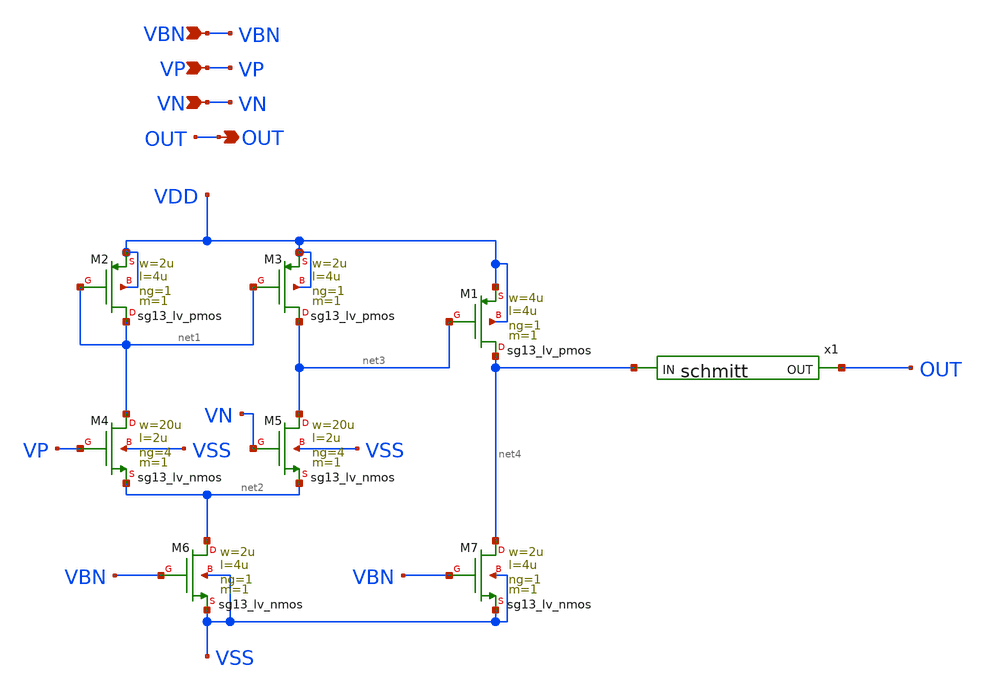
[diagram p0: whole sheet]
** sch_path: design/blocks/comparator/schematic/comp_sup.sch
**.subckt comp_sup OUT VN VP VBN
*.opin OUT
*.ipin VN
*.ipin VP
*.ipin VBN
XM2 net1 net1 VDD VDD sg13_lv_pmos w=2u l=4u ng=1 m=1 mm_ok=1
XM3 net3 net1 VDD VDD sg13_lv_pmos w=2u l=4u ng=1 m=1 mm_ok=1
XM4 net1 VP net2 VSS sg13_lv_nmos w=20u l=2u ng=4 m=1 mm_ok=1
XM5 net3 VN net2 VSS sg13_lv_nmos w=20u l=2u ng=4 m=1 mm_ok=1
XM6 net2 VBN VSS VSS sg13_lv_nmos w=2u l=4u ng=1 m=1 mm_ok=1
XM1 net4 net3 VDD VDD sg13_lv_pmos w=4u l=4u ng=1 m=1 mm_ok=1
XM7 net4 VBN VSS VSS sg13_lv_nmos w=2u l=4u ng=1 m=1 mm_ok=1
x1 net4 OUT VDD VSS schmitt
**.ends

* expanding   symbol:  schmitt.sym # of pins=2
** sym_path: design/blocks/schmitt/schematic/schmitt.sym
** sch_path: design/blocks/schmitt/schematic/schmitt.sch
.subckt schmitt IN OUT VDD VSS
*.opin OUT
*.ipin IN
XM4 net1 IN VDD VDD sg13_lv_pmos w=1.04u l=0.13u ng=1 m=1 mm_ok=1
XM6 OUT IN net2 VSS sg13_lv_nmos w=0.76u l=0.13u ng=1 m=1 mm_ok=1
XM5 OUT IN net1 VDD sg13_lv_pmos w=1.04u l=0.13u ng=1 m=1 mm_ok=1
XM7 net2 IN VSS VSS sg13_lv_nmos w=0.76u l=0.13u ng=1 m=1 mm_ok=1
XM8 VSS OUT net1 VDD sg13_lv_pmos w=0.42u l=0.13u ng=1 m=1 mm_ok=1
XM9 VDD OUT net2 VSS sg13_lv_nmos w=0.42u l=0.13u ng=1 m=1 mm_ok=1
.ends

.end
